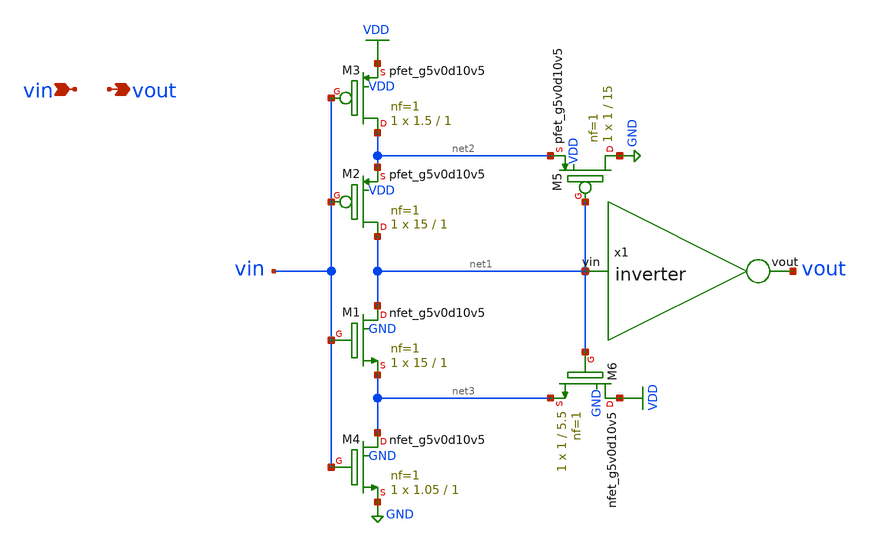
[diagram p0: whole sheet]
** sch_path: schematics/schmitt_trigger.sch
**.subckt schmitt_trigger vin vout
*.ipin vin
*.opin vout
XM1 net1 vin net3 GND sky130_fd_pr__nfet_g5v0d10v5 L=1 W=15 nf=1 ad='int((nf+1)/2) * W/nf * 0.29' as='int((nf+2)/2) * W/nf * 0.29'
+ pd='2*int((nf+1)/2) * (W/nf + 0.29)' ps='2*int((nf+2)/2) * (W/nf + 0.29)' nrd='0.29 / W' nrs='0.29 / W'
+ sa=0 sb=0 sd=0 mult=1 m=1
XM2 net1 vin net2 VDD sky130_fd_pr__pfet_g5v0d10v5 L=1 W=15 nf=1 ad='int((nf+1)/2) * W/nf * 0.29' as='int((nf+2)/2) * W/nf * 0.29'
+ pd='2*int((nf+1)/2) * (W/nf + 0.29)' ps='2*int((nf+2)/2) * (W/nf + 0.29)' nrd='0.29 / W' nrs='0.29 / W'
+ sa=0 sb=0 sd=0 mult=1 m=1
XM3 net2 vin VDD VDD sky130_fd_pr__pfet_g5v0d10v5 L=1 W=1.5 nf=1 ad='int((nf+1)/2) * W/nf * 0.29' as='int((nf+2)/2) * W/nf * 0.29'
+ pd='2*int((nf+1)/2) * (W/nf + 0.29)' ps='2*int((nf+2)/2) * (W/nf + 0.29)' nrd='0.29 / W' nrs='0.29 / W'
+ sa=0 sb=0 sd=0 mult=1 m=1
XM4 net3 vin GND GND sky130_fd_pr__nfet_g5v0d10v5 L=1 W=1.05 nf=1 ad='int((nf+1)/2) * W/nf * 0.29' as='int((nf+2)/2) * W/nf * 0.29'
+ pd='2*int((nf+1)/2) * (W/nf + 0.29)' ps='2*int((nf+2)/2) * (W/nf + 0.29)' nrd='0.29 / W' nrs='0.29 / W'
+ sa=0 sb=0 sd=0 mult=1 m=1
XM5 GND net1 net2 VDD sky130_fd_pr__pfet_g5v0d10v5 L=15 W=1 nf=1 ad='int((nf+1)/2) * W/nf * 0.29' as='int((nf+2)/2) * W/nf * 0.29'
+ pd='2*int((nf+1)/2) * (W/nf + 0.29)' ps='2*int((nf+2)/2) * (W/nf + 0.29)' nrd='0.29 / W' nrs='0.29 / W'
+ sa=0 sb=0 sd=0 mult=1 m=1
XM6 VDD net1 net3 GND sky130_fd_pr__nfet_g5v0d10v5 L=5.5 W=1 nf=1 ad='int((nf+1)/2) * W/nf * 0.29' as='int((nf+2)/2) * W/nf * 0.29'
+ pd='2*int((nf+1)/2) * (W/nf + 0.29)' ps='2*int((nf+2)/2) * (W/nf + 0.29)' nrd='0.29 / W' nrs='0.29 / W'
+ sa=0 sb=0 sd=0 mult=1 m=1
x1 vout net1 inverter
**.ends

* expanding   symbol:  /media/sf_share/final_project/inverter.sym # of pins=2
** sym_path: schematics/inverter.sym
** sch_path: schematics/inverter.sch
.subckt inverter vout vin
*.ipin vin
*.opin vout
XM3 vout vin VDD VDD sky130_fd_pr__pfet_g5v0d10v5 L=0.5 W=0.5 nf=1 ad='int((nf+1)/2) * W/nf * 0.29' as='int((nf+2)/2) * W/nf * 0.29'
+ pd='2*int((nf+1)/2) * (W/nf + 0.29)' ps='2*int((nf+2)/2) * (W/nf + 0.29)' nrd='0.29 / W' nrs='0.29 / W'
+ sa=0 sb=0 sd=0 mult=1 m=1
XM5 vout vin GND GND sky130_fd_pr__nfet_g5v0d10v5 L=0.5 W=0.5 nf=1 ad='int((nf+1)/2) * W/nf * 0.29' as='int((nf+2)/2) * W/nf * 0.29'
+ pd='2*int((nf+1)/2) * (W/nf + 0.29)' ps='2*int((nf+2)/2) * (W/nf + 0.29)' nrd='0.29 / W' nrs='0.29 / W'
+ sa=0 sb=0 sd=0 mult=1 m=1
.ends

.GLOBAL GND
.GLOBAL VDD
.end
